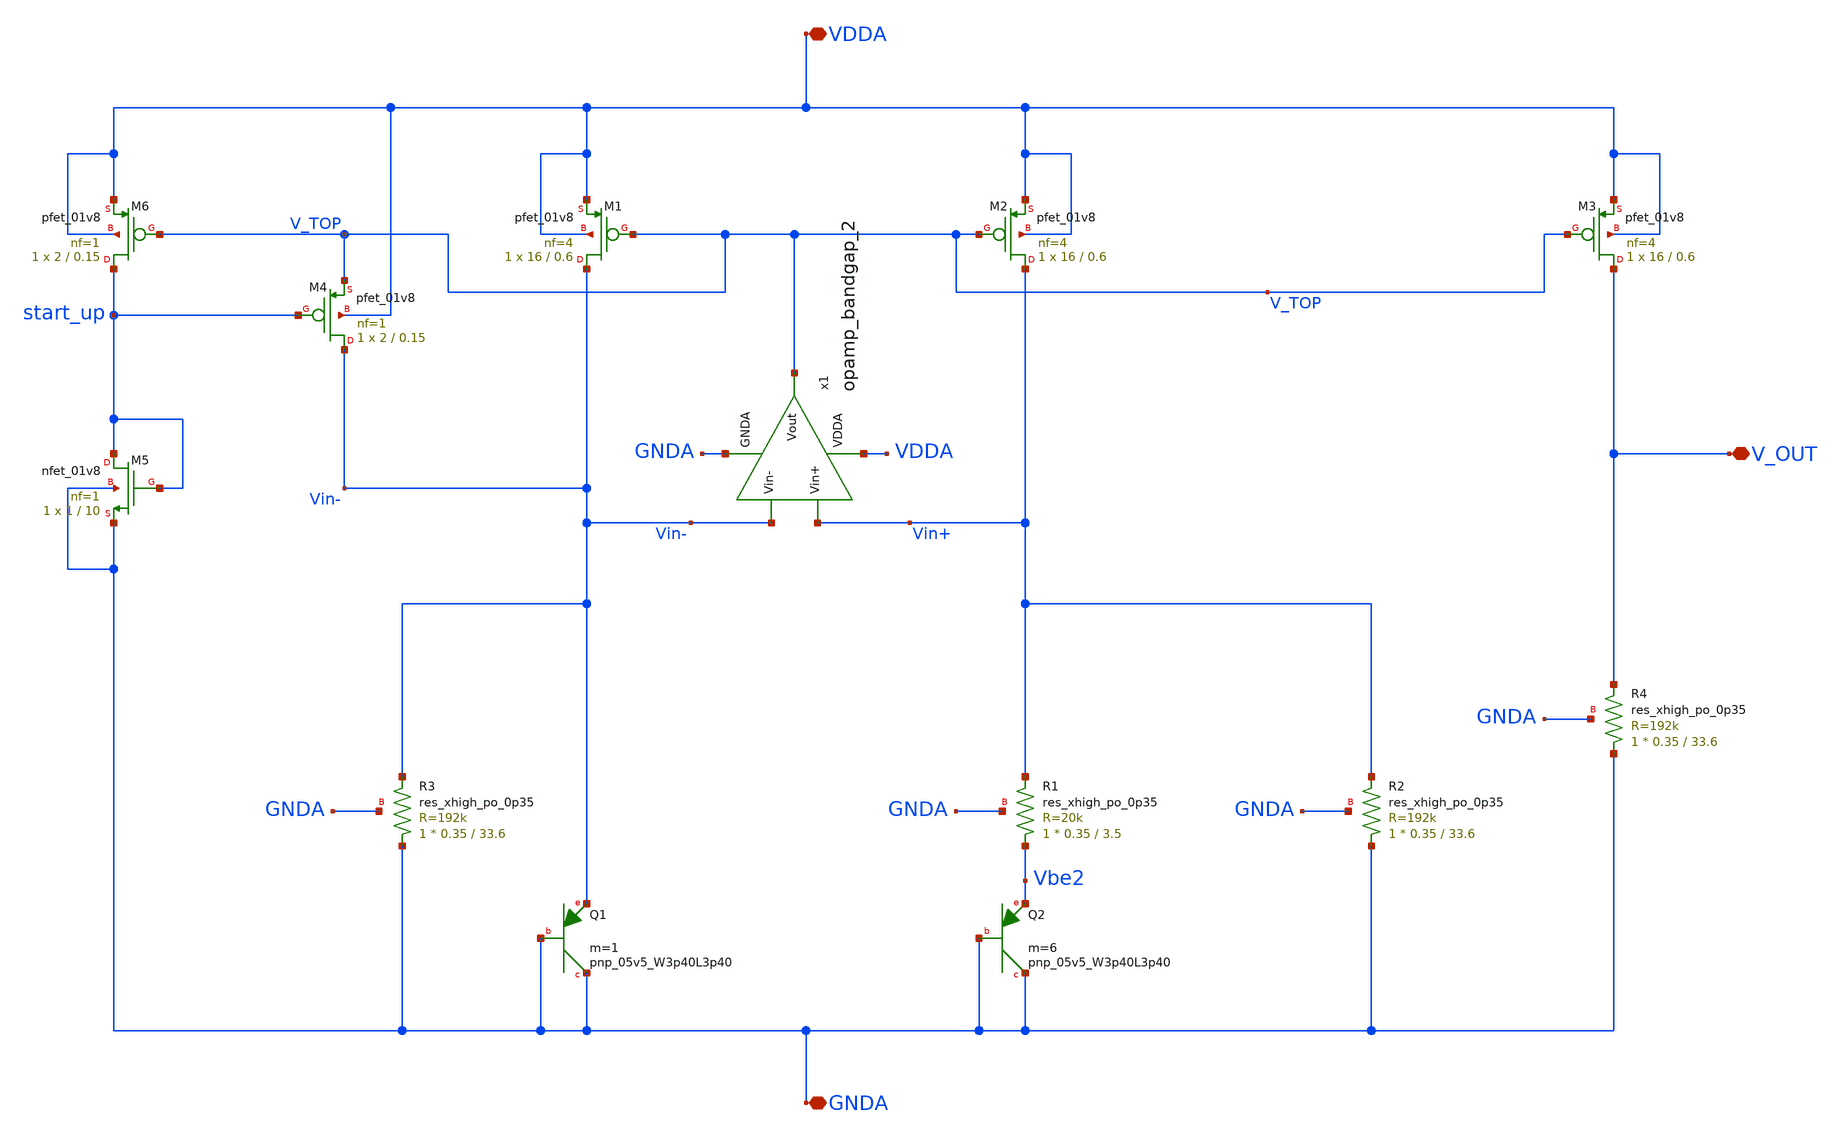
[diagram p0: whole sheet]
** sch_path: projects/bandgapref/xschem_ngspice/new_files/low_voltage_BGR.sch
**.subckt low_voltage_BGR VDDA GNDA V_OUT
*.iopin VDDA
*.iopin GNDA
*.iopin V_OUT
XQ1 GNDA GNDA Vin- sky130_fd_pr__pnp_05v5_W3p40L3p40 m=1
XQ2 GNDA GNDA Vbe2 sky130_fd_pr__pnp_05v5_W3p40L3p40 m=6
XM1 Vin- V_TOP VDDA VDDA sky130_fd_pr__pfet_01v8 L=0.6 W=16 nf=4 ad='int((nf+1)/2) * W/nf * 0.29' as='int((nf+2)/2) * W/nf * 0.29'
+ pd='2*int((nf+1)/2) * (W/nf + 0.29)' ps='2*int((nf+2)/2) * (W/nf + 0.29)' nrd='0.29 / W' nrs='0.29 / W'
+ sa=0 sb=0 sd=0 mult=1 m=1
XM2 Vin+ V_TOP VDDA VDDA sky130_fd_pr__pfet_01v8 L=0.6 W=16 nf=4 ad='int((nf+1)/2) * W/nf * 0.29' as='int((nf+2)/2) * W/nf * 0.29'
+ pd='2*int((nf+1)/2) * (W/nf + 0.29)' ps='2*int((nf+2)/2) * (W/nf + 0.29)' nrd='0.29 / W' nrs='0.29 / W'
+ sa=0 sb=0 sd=0 mult=1 m=1
XM3 V_OUT V_TOP VDDA VDDA sky130_fd_pr__pfet_01v8 L=0.6 W=16 nf=4 ad='int((nf+1)/2) * W/nf * 0.29' as='int((nf+2)/2) * W/nf * 0.29'
+ pd='2*int((nf+1)/2) * (W/nf + 0.29)' ps='2*int((nf+2)/2) * (W/nf + 0.29)' nrd='0.29 / W' nrs='0.29 / W'
+ sa=0 sb=0 sd=0 mult=1 m=1
XR1 Vbe2 Vin+ GNDA sky130_fd_pr__res_xhigh_po_0p35 L=3.5 mult=1 m=1
XR2 GNDA Vin+ GNDA sky130_fd_pr__res_xhigh_po_0p35 L=33.6 mult=1 m=1
XR3 GNDA Vin- GNDA sky130_fd_pr__res_xhigh_po_0p35 L=33.6 mult=1 m=1
XR4 GNDA V_OUT GNDA sky130_fd_pr__res_xhigh_po_0p35 L=33.6 mult=1 m=1
XM5 start_up start_up GNDA GNDA sky130_fd_pr__nfet_01v8 L=10 W=1 nf=1 ad='int((nf+1)/2) * W/nf * 0.29'
+ as='int((nf+2)/2) * W/nf * 0.29' pd='2*int((nf+1)/2) * (W/nf + 0.29)' ps='2*int((nf+2)/2) * (W/nf + 0.29)'
+ nrd='0.29 / W' nrs='0.29 / W' sa=0 sb=0 sd=0 mult=1 m=1
XM6 start_up V_TOP VDDA VDDA sky130_fd_pr__pfet_01v8 L=0.15 W=2 nf=1 ad='int((nf+1)/2) * W/nf * 0.29'
+ as='int((nf+2)/2) * W/nf * 0.29' pd='2*int((nf+1)/2) * (W/nf + 0.29)' ps='2*int((nf+2)/2) * (W/nf + 0.29)'
+ nrd='0.29 / W' nrs='0.29 / W' sa=0 sb=0 sd=0 mult=1 m=1
XM4 Vin- start_up V_TOP VDDA sky130_fd_pr__pfet_01v8 L=0.15 W=2 nf=1 ad='int((nf+1)/2) * W/nf * 0.29'
+ as='int((nf+2)/2) * W/nf * 0.29' pd='2*int((nf+1)/2) * (W/nf + 0.29)' ps='2*int((nf+2)/2) * (W/nf + 0.29)'
+ nrd='0.29 / W' nrs='0.29 / W' sa=0 sb=0 sd=0 mult=1 m=1
x1 VDDA V_TOP Vin- Vin+ GNDA opamp_bandgap_2
**.ends

* expanding   symbol:
*+  /foss/designs/projects/bandgapref/xschem_ngspice/new_files/opamp_bandgap_2.sym # of pins=5
** sym_path: projects/bandgapref/xschem_ngspice/new_files/opamp_bandgap_2.sym
** sch_path: projects/bandgapref/xschem_ngspice/new_files/opamp_bandgap_2.sch
.subckt opamp_bandgap_2 VDDA Vout Vin- Vin+ GNDA
*.ipin Vin+
*.opin Vout
*.ipin Vin-
*.ipin GNDA
*.ipin VDDA
XM1 V_p V_mirror GNDA GNDA sky130_fd_pr__nfet_01v8 L=10 W=10 nf=1 ad='int((nf+1)/2) * W/nf * 0.29' as='int((nf+2)/2) * W/nf * 0.29'
+ pd='2*int((nf+1)/2) * (W/nf + 0.29)' ps='2*int((nf+2)/2) * (W/nf + 0.29)' nrd='0.29 / W' nrs='0.29 / W'
+ sa=0 sb=0 sd=0 mult=1 m=1
XM2 V_mirror Vin- V_p GNDA sky130_fd_pr__nfet_01v8 L=1.2 W=10 nf=1 ad='int((nf+1)/2) * W/nf * 0.29' as='int((nf+2)/2) * W/nf * 0.29'
+ pd='2*int((nf+1)/2) * (W/nf + 0.29)' ps='2*int((nf+2)/2) * (W/nf + 0.29)' nrd='0.29 / W' nrs='0.29 / W'
+ sa=0 sb=0 sd=0 mult=1 m=1
XM3 1st_Vout Vin+ V_p GNDA sky130_fd_pr__nfet_01v8 L=1.2 W=10 nf=1 ad='int((nf+1)/2) * W/nf * 0.29' as='int((nf+2)/2) * W/nf * 0.29'
+ pd='2*int((nf+1)/2) * (W/nf + 0.29)' ps='2*int((nf+2)/2) * (W/nf + 0.29)' nrd='0.29 / W' nrs='0.29 / W'
+ sa=0 sb=0 sd=0 mult=1 m=1
XM4 V_mirror V_mirror VDDA VDDA sky130_fd_pr__pfet_01v8 L=1.2 W=20 nf=2 ad='int((nf+1)/2) * W/nf * 0.29'
+ as='int((nf+2)/2) * W/nf * 0.29' pd='2*int((nf+1)/2) * (W/nf + 0.29)' ps='2*int((nf+2)/2) * (W/nf + 0.29)'
+ nrd='0.29 / W' nrs='0.29 / W' sa=0 sb=0 sd=0 mult=1 m=1
XM5 1st_Vout V_mirror VDDA VDDA sky130_fd_pr__pfet_01v8 L=1.2 W=20 nf=2 ad='int((nf+1)/2) * W/nf * 0.29'
+ as='int((nf+2)/2) * W/nf * 0.29' pd='2*int((nf+1)/2) * (W/nf + 0.29)' ps='2*int((nf+2)/2) * (W/nf + 0.29)'
+ nrd='0.29 / W' nrs='0.29 / W' sa=0 sb=0 sd=0 mult=1 m=1
XM6 Vout V_mirror GNDA GNDA sky130_fd_pr__nfet_01v8 L=10 W=10 nf=1 ad='int((nf+1)/2) * W/nf * 0.29' as='int((nf+2)/2) * W/nf * 0.29'
+ pd='2*int((nf+1)/2) * (W/nf + 0.29)' ps='2*int((nf+2)/2) * (W/nf + 0.29)' nrd='0.29 / W' nrs='0.29 / W'
+ sa=0 sb=0 sd=0 mult=1 m=1
XM7 Vout 1st_Vout VDDA VDDA sky130_fd_pr__pfet_01v8 L=1.2 W=20 nf=2 ad='int((nf+1)/2) * W/nf * 0.29'
+ as='int((nf+2)/2) * W/nf * 0.29' pd='2*int((nf+1)/2) * (W/nf + 0.29)' ps='2*int((nf+2)/2) * (W/nf + 0.29)'
+ nrd='0.29 / W' nrs='0.29 / W' sa=0 sb=0 sd=0 mult=1 m=1
.ends

.end
